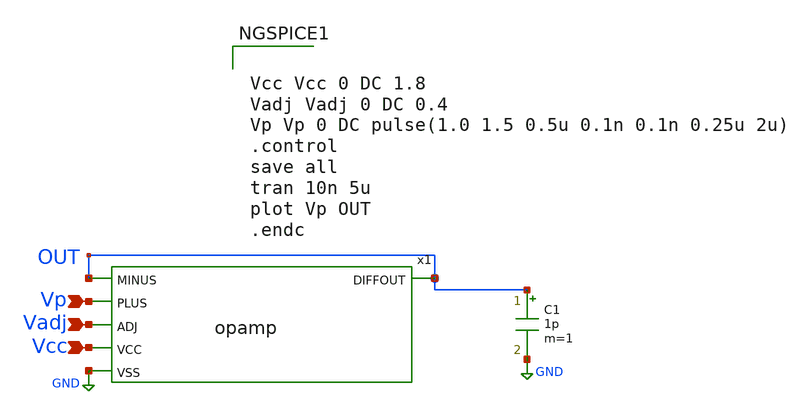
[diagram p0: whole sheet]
** sch_path: schematic/test_step.sch
**.subckt test_step Vp Vadj Vcc
*.ipin Vp
*.ipin Vadj
*.ipin Vcc
C1 OUT GND 1p m=1
x1 OUT OUT Vp Vadj Vcc GND opamp
**** begin user architecture code

** opencircuitdesign pdks install
.lib $::SKYWATER_MODELS/sky130.lib.spice tt




Vcc Vcc 0 DC 1.8
Vadj Vadj 0 DC 0.4
Vp Vp 0 DC pulse(1.0 1.5 0.5u 0.1n 0.1n 0.25u 2u)
.control
save all
tran 10n 5u
plot Vp OUT
.endc


**** end user architecture code
**.ends

* expanding   symbol:  opamp.sym # of pins=6
** sym_path: schematic/opamp.sym
** sch_path: schematic/opamp.sch
.subckt opamp DIFFOUT MINUS PLUS ADJ VCC VSS
*.ipin PLUS
*.ipin MINUS
*.ipin VSS
*.ipin VCC
*.opin DIFFOUT
*.ipin ADJ
C6 G1 0 2f m=1
XM18 G2 G2 net6 VSS sky130_fd_pr__nfet_01v8_lvt L=4 W=2 nf=1 ad='W * 0.29' as='W * 0.29' pd='2*(W + 0.29)'
+ ps='2*(W + 0.29)' nrd=0 nrs=0 sa=0 sb=0 sd=0 mult=1 m=1
XM2 G1 G1 net7 VSS sky130_fd_pr__nfet_01v8_lvt L=4 W=2 nf=1 ad='W * 0.29' as='W * 0.29' pd='2*(W + 0.29)'
+ ps='2*(W + 0.29)' nrd=0 nrs=0 sa=0 sb=0 sd=0 mult=1 m=1
XMR G2 PLUS net8 VCC sky130_fd_pr__pfet_01v8_lvt L=2 W=8 nf=1 ad='W * 0.29' as='W * 0.29' pd='2*(W + 0.29)'
+ ps='2*(W + 0.29)' nrd=0 nrs=0 sa=0 sb=0 sd=0 mult=1 m=1
XML G1 MINUS net9 VCC sky130_fd_pr__pfet_01v8_lvt L=2 W=8 nf=1 ad='W * 0.29' as='W * 0.29' pd='2*(W + 0.29)'
+ ps='2*(W + 0.29)' nrd=0 nrs=0 sa=0 sb=0 sd=0 mult=1 m=1
v1 SP net9 0
.save i(v1)
C4 SP 0 2f m=1
C1 G2 0 2f m=1
C5 DIFFOUT 0 4f m=1
XM6 DIFFOUT G2 net1 VSS sky130_fd_pr__nfet_01v8_lvt L=4 W=2 nf=1 ad='W * 0.29' as='W * 0.29' pd='2*(W + 0.29)'
+ ps='2*(W + 0.29)' nrd=0 nrs=0 sa=0 sb=0 sd=0 mult=1 m=1
v2 SP net8 0
.save i(v2)
v4 net1 VSS 0
.save i(v4)
v6 VCC SP 0
.save i(v6)
v17 VCC net3 0
.save i(v17)
XM12 net2 G1 VSS VSS sky130_fd_pr__nfet_01v8_lvt L=4 W=2 nf=1 ad='W * 0.29' as='W * 0.29' pd='2*(W + 0.29)'
+ ps='2*(W + 0.29)' nrd=0 nrs=0 sa=0 sb=0 sd=0 mult=1 m=1
XM54 net2 net2 net3 VCC sky130_fd_pr__pfet_01v8_lvt L=4 W=4 nf=1 ad='W * 0.29' as='W * 0.29' pd='2*(W + 0.29)'
+ ps='2*(W + 0.29)' nrd=0 nrs=0 sa=0 sb=0 sd=0 mult=1 m=1
XM5 DIFFOUT net2 net3 VCC sky130_fd_pr__pfet_01v8_lvt L=4 W=4 nf=1 ad='W * 0.29' as='W * 0.29' pd='2*(W + 0.29)'
+ ps='2*(W + 0.29)' nrd=0 nrs=0 sa=0 sb=0 sd=0 mult=1 m=1
XM8 net4 ADJ VCC VCC sky130_fd_pr__pfet_01v8_lvt L=1 W=1 nf=1 ad='W * 0.29' as='W * 0.29' pd='W + 2 * 0.29'
+ ps='W + 2 * 0.29' nrd=0 nrs=0 sa=0 sb=0 sd=0 mult=1 m=1
XM9 net4 ADJ net5 VSS sky130_fd_pr__nfet_01v8_lvt L=1 W=0.5 nf=1 ad='W * 0.29' as='W * 0.29' pd='W + 2 * 0.29'
+ ps='W + 2 * 0.29' nrd=0 nrs=0 sa=0 sb=0 sd=0 mult=1 m=1
XM10 net5 VCC VSS VSS sky130_fd_pr__nfet_01v8_lvt L=8 W=0.5 nf=1 ad='W * 0.29' as='W * 0.29' pd='2*(W + 0.29)'
+ ps='2*(W + 0.29)' nrd=0 nrs=0 sa=0 sb=0 sd=0 mult=1 m=1
v3 net4 G1 0
.save i(v3)
v5 net6 VSS 0
.save i(v5)
v7 net7 VSS 0
.save i(v7)
.ends

.GLOBAL GND
.end
